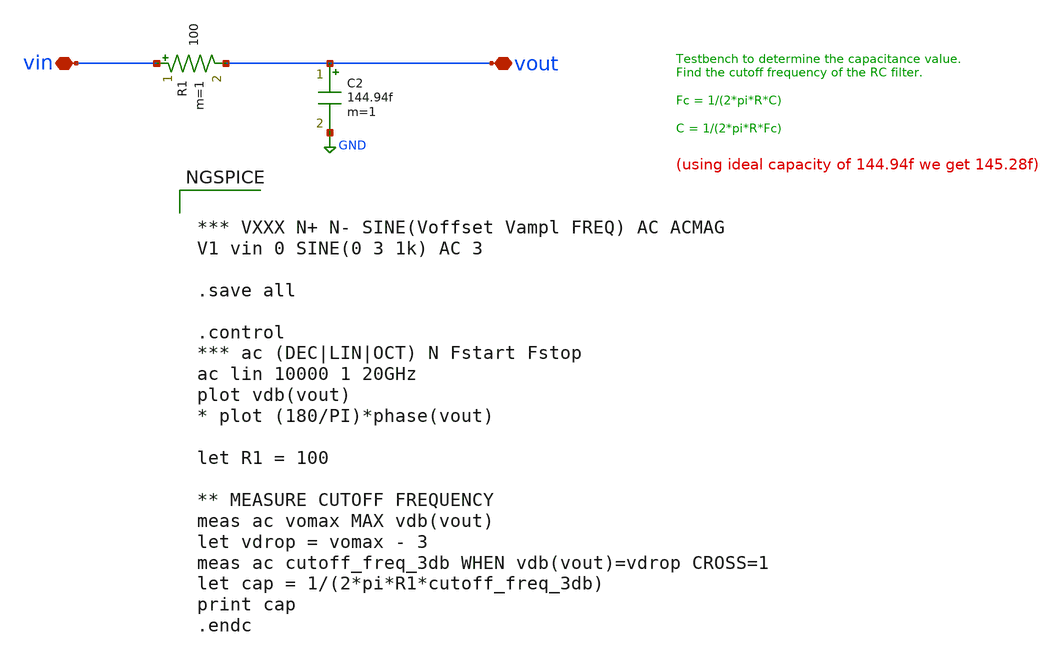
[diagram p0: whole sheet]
** sch_path: testdata/designs/sky130A/cap_vpp_11p5x11p7_l1m1m2m3m4_shieldm5/cap_vpp_11p5x11p7_l1m1m2m3m4_shieldm5__checkWithStdCap_tb.sch
**.subckt cap_vpp_11p5x11p7_l1m1m2m3m4_shieldm5__checkWithStdCap_tb vin vout
*.iopin vin
*.iopin vout
R1 vin vout 100 m=1
C2 vout GND 144.94f m=1
**** begin user architecture code


*** VXXX N+ N- SINE(Voffset Vampl FREQ) AC ACMAG
V1 vin 0 SINE(0 3 1k) AC 3

.save all

.control
*** ac (DEC|LIN|OCT) N Fstart Fstop
ac lin 10000 1 20GHz
plot vdb(vout)
* plot (180/PI)*phase(vout)

let R1 = 100

** MEASURE CUTOFF FREQUENCY
meas ac vomax MAX vdb(vout)
let vdrop = vomax - 3
meas ac cutoff_freq_3db WHEN vdb(vout)=vdrop CROSS=1
let cap = 1/(2*pi*R1*cutoff_freq_3db)
print cap
.endc



** opencircuitdesign pdks install
.lib $::SKYWATER_MODELS/sky130.lib.spice tt


**** end user architecture code
**.ends
.GLOBAL GND
.end
